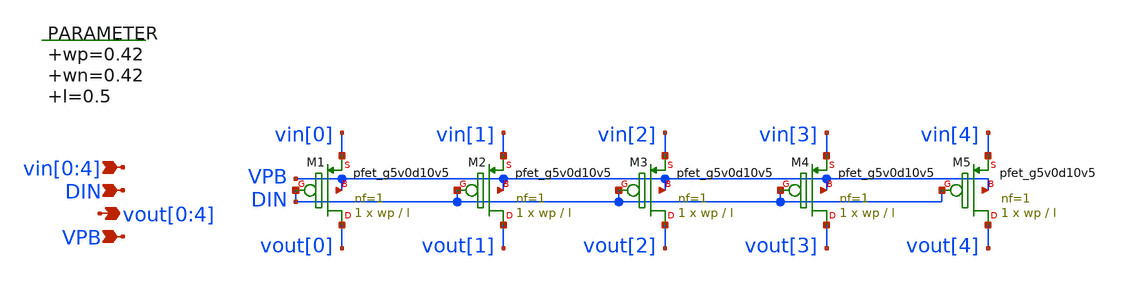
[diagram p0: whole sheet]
** sch_path: xschem/switch_pmos_1g_5o.sch
**.subckt switch_pmos_1g_5o vin[0],vin[1],vin[2],vin[3],vin[4]
*+ vout[0],vout[1],vout[2],vout[3],vout[4] VPB DIN
*.ipin vin[0],vin[1],vin[2],vin[3],vin[4]
*.opin vout[0],vout[1],vout[2],vout[3],vout[4]
*.ipin VPB
*.ipin DIN
.param wp=0.42 wn=0.42 l=0.5

XM1 vout[0] DIN vin[0] VPB sky130_fd_pr__pfet_g5v0d10v5 L=l W=wp nf=1 ad='int((nf+1)/2) * W/nf * 0.29'
+ as='int((nf+2)/2) * W/nf * 0.29' pd='2*int((nf+1)/2) * (W/nf + 0.29)' ps='2*int((nf+2)/2) * (W/nf + 0.29)'
+ nrd='0.29 / W' nrs='0.29 / W' sa=0 sb=0 sd=0 mult=1 m=1
XM2 vout[1] DIN vin[1] VPB sky130_fd_pr__pfet_g5v0d10v5 L=l W=wp nf=1 ad='int((nf+1)/2) * W/nf * 0.29'
+ as='int((nf+2)/2) * W/nf * 0.29' pd='2*int((nf+1)/2) * (W/nf + 0.29)' ps='2*int((nf+2)/2) * (W/nf + 0.29)'
+ nrd='0.29 / W' nrs='0.29 / W' sa=0 sb=0 sd=0 mult=1 m=1
XM3 vout[2] DIN vin[2] VPB sky130_fd_pr__pfet_g5v0d10v5 L=l W=wp nf=1 ad='int((nf+1)/2) * W/nf * 0.29'
+ as='int((nf+2)/2) * W/nf * 0.29' pd='2*int((nf+1)/2) * (W/nf + 0.29)' ps='2*int((nf+2)/2) * (W/nf + 0.29)'
+ nrd='0.29 / W' nrs='0.29 / W' sa=0 sb=0 sd=0 mult=1 m=1
XM4 vout[3] DIN vin[3] VPB sky130_fd_pr__pfet_g5v0d10v5 L=l W=wp nf=1 ad='int((nf+1)/2) * W/nf * 0.29'
+ as='int((nf+2)/2) * W/nf * 0.29' pd='2*int((nf+1)/2) * (W/nf + 0.29)' ps='2*int((nf+2)/2) * (W/nf + 0.29)'
+ nrd='0.29 / W' nrs='0.29 / W' sa=0 sb=0 sd=0 mult=1 m=1
XM5 vout[4] DIN vin[4] VPB sky130_fd_pr__pfet_g5v0d10v5 L=l W=wp nf=1 ad='int((nf+1)/2) * W/nf * 0.29'
+ as='int((nf+2)/2) * W/nf * 0.29' pd='2*int((nf+1)/2) * (W/nf + 0.29)' ps='2*int((nf+2)/2) * (W/nf + 0.29)'
+ nrd='0.29 / W' nrs='0.29 / W' sa=0 sb=0 sd=0 mult=1 m=1
**.ends
.end
